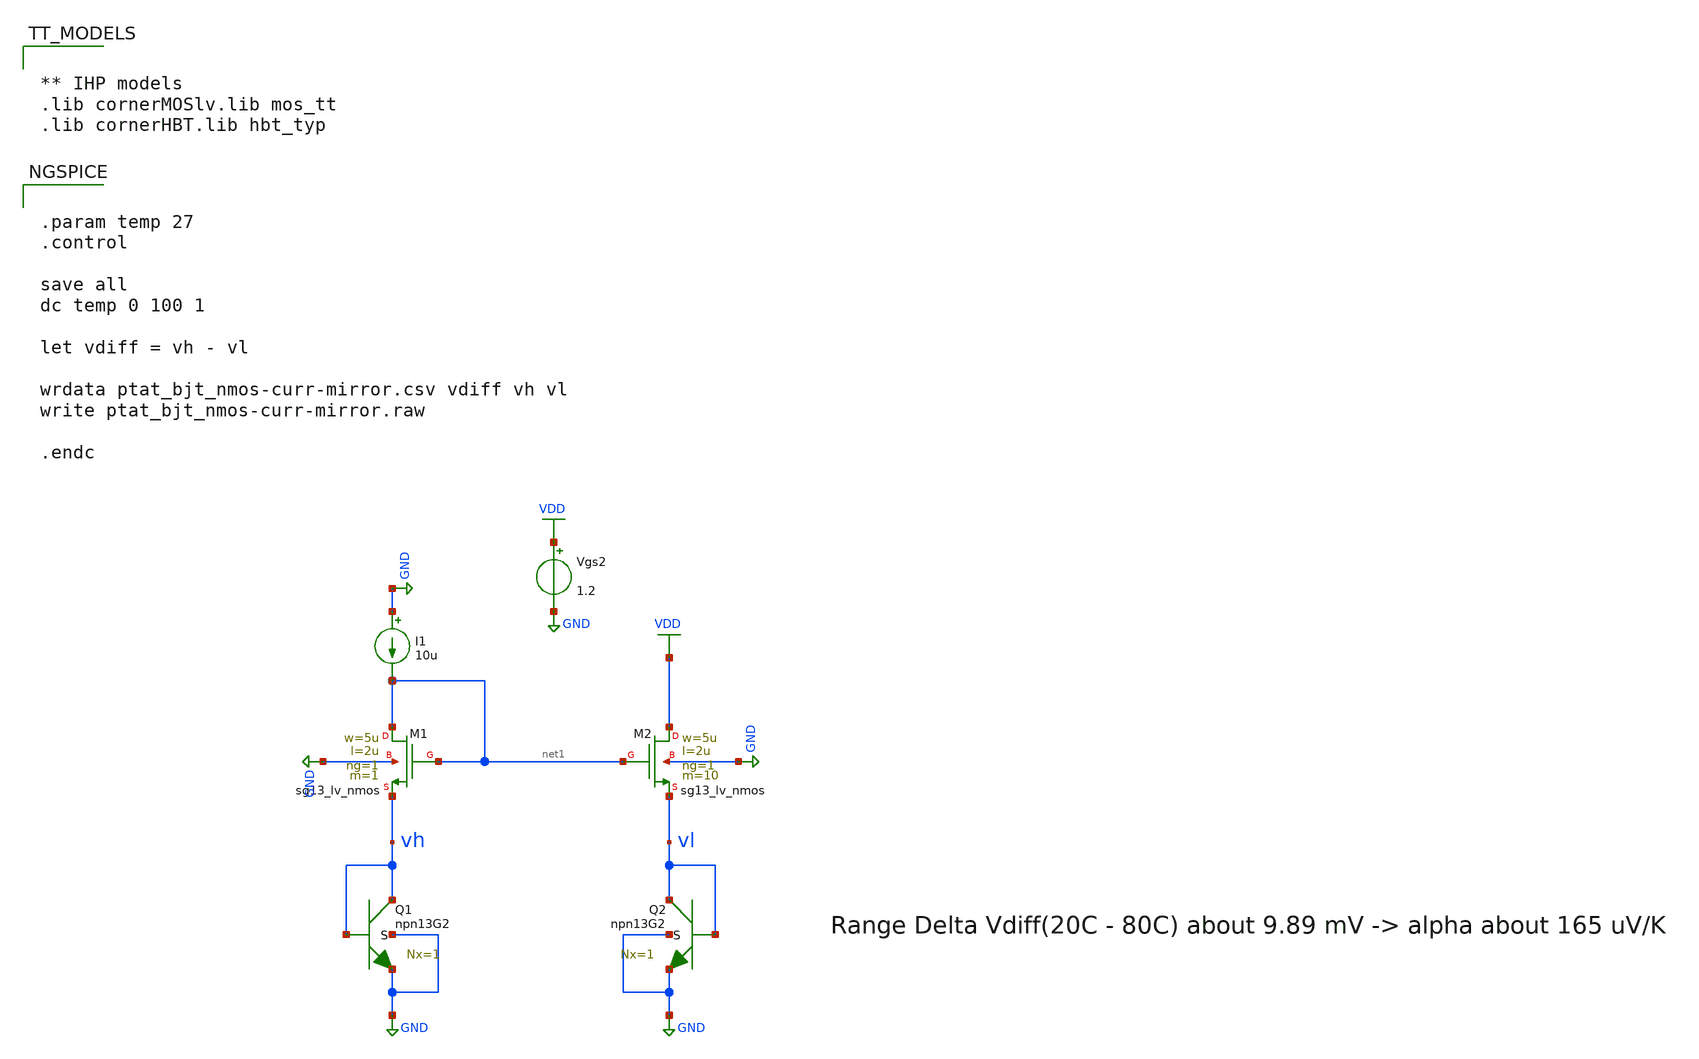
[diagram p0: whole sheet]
** sch_path: TempSensor/design_data/xschem/ptat_bjt_nmos-curr-mirror.sch
* Copyright 2023 IHP PDK Authors
**.subckt ptat_bjt_nmos-curr-mirror
XM1 net1 net1 vh GND sg13_lv_nmos w=5u l=2u ng=1 m=1 mm_ok=1
XM2 VDD net1 vl GND sg13_lv_nmos w=5u l=2u ng=1 m=10 mm_ok=1
I1 GND net1 10u
Vgs2 VDD GND 1.2
XQ1 vh vh GND GND npn13G2 Nx=1 mm_ok=1
XQ2 vl vl GND GND npn13G2 Nx=1 mm_ok=1
**** begin user architecture code


.param temp 27
.control

save all
dc temp 0 100 1

let vdiff = vh - vl

wrdata ptat_bjt_nmos-curr-mirror.csv vdiff vh vl
write ptat_bjt_nmos-curr-mirror.raw

.endc




** IHP models
.lib cornerMOSlv.lib mos_tt
.lib cornerHBT.lib hbt_typ


**** end user architecture code
**.ends
.GLOBAL GND
.GLOBAL VDD
.end
